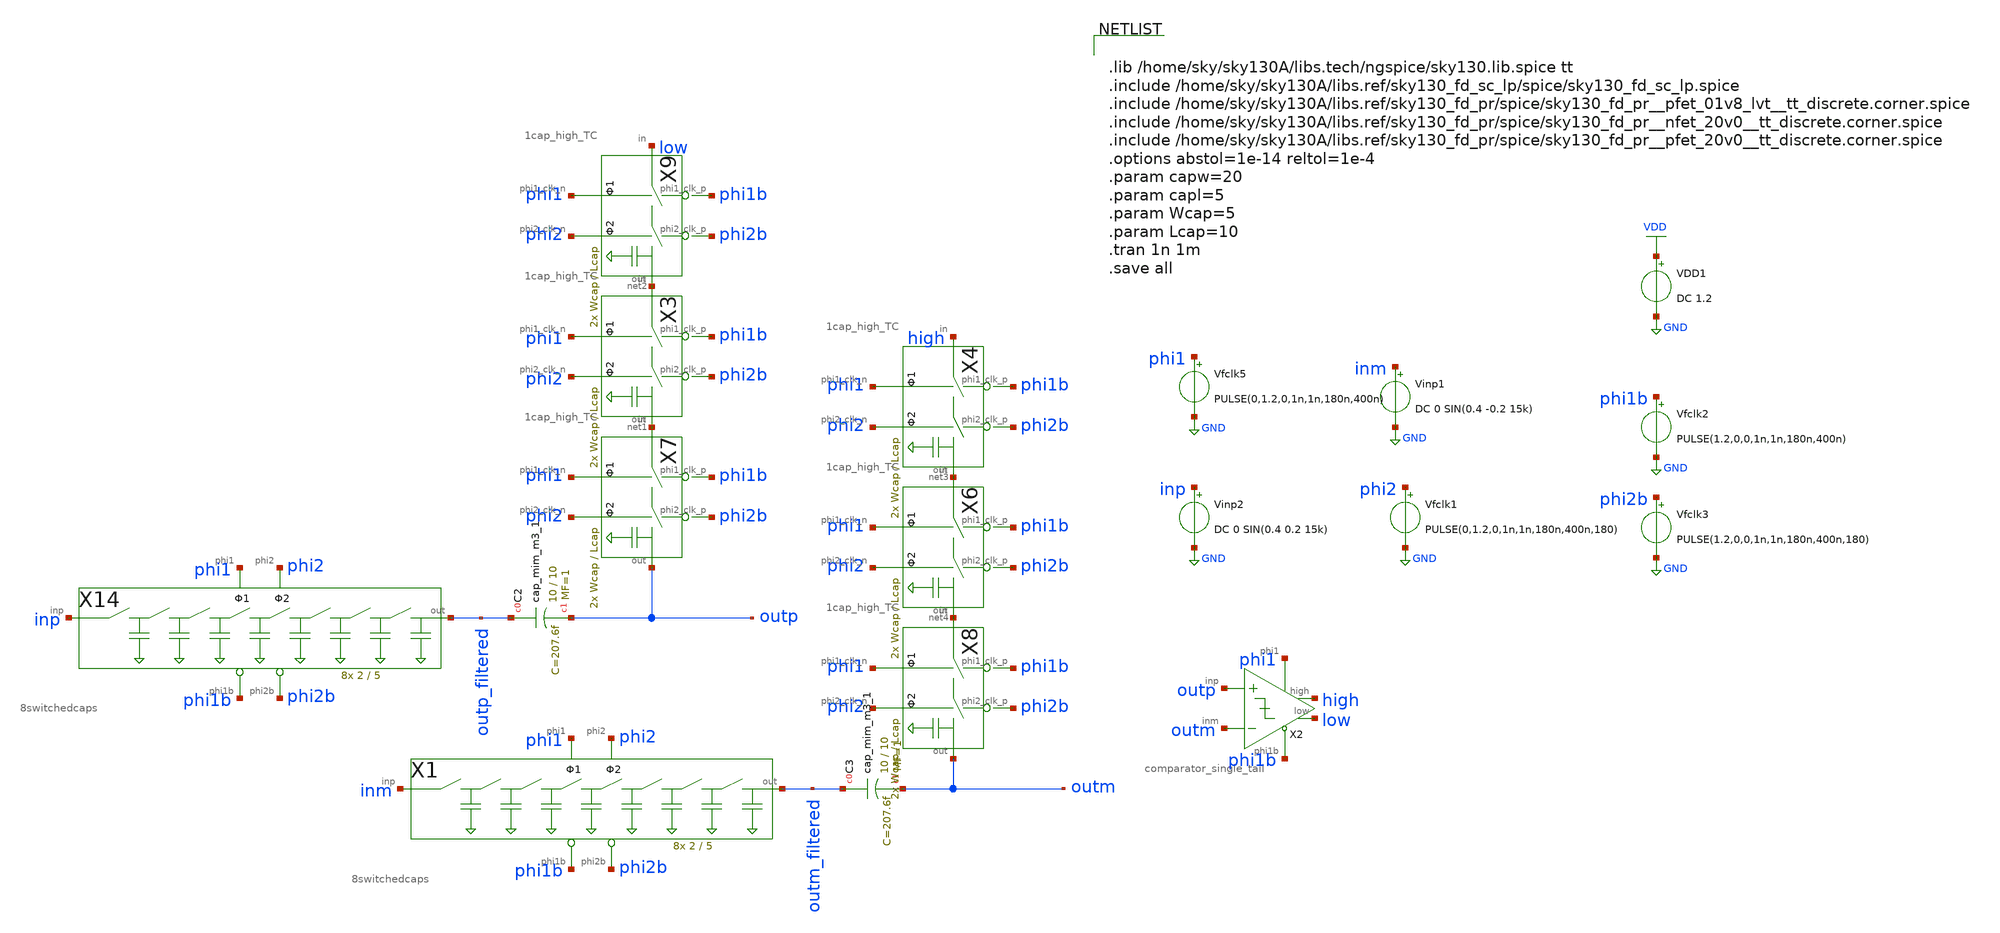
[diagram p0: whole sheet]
** sch_path: xschem/archive/comparator_latest/3cao_com_tb_az.sch
**.subckt 3cao_com_tb_az
VDD1 VDD GND DC 1.2
Vfclk5 phi1 GND PULSE(0,1.2,0,1n,1n,180n,400n)
Vfclk1 phi2 GND PULSE(0,1.2,0,1n,1n,180n,400n,180)
Vfclk2 phi1b GND PULSE(1.2,0,0,1n,1n,180n,400n)
Vfclk3 phi2b GND PULSE(1.2,0,0,1n,1n,180n,400n,180)
Vinp2 inp GND DC 0 SIN(0.4 0.2 15k)
Vinp1 inm GND DC 0 SIN(0.4 -0.2 15k)
XC2 outp_filtered outp sky130_fd_pr__cap_mim_m3_1 W=10 L=10 MF=1 m=1
XC3 outm_filtered outm sky130_fd_pr__cap_mim_m3_1 W=10 L=10 MF=1 m=1
X14 inp outp_filtered phi2 phi1 phi1b phi2b 8switchedcaps Wcap=2 Lcap=5
X1 inm outm_filtered phi2 phi1 phi1b phi2b 8switchedcaps Wcap=2 Lcap=5
X7 net1 outp phi2 phi1 phi1b phi2b 1cap_high_TC Wcap=Wcap Lcap=Lcap
X3 net2 net1 phi2 phi1 phi1b phi2b 1cap_high_TC Wcap=Wcap Lcap=Lcap
X4 high net3 phi2 phi1 phi1b phi2b 1cap_high_TC Wcap=Wcap Lcap=Lcap
X6 net3 net4 phi2 phi1 phi1b phi2b 1cap_high_TC Wcap=Wcap Lcap=Lcap
X8 net4 outm phi2 phi1 phi1b phi2b 1cap_high_TC Wcap=Wcap Lcap=Lcap
X9 low net2 phi2 phi1 phi1b phi2b 1cap_high_TC Wcap=Wcap Lcap=Lcap
X2 outp outm high phi1 phi1b low comparator_single_tail Wplus=0.42 Lplus=0.42 Wminus=0.42
+ Lminus=0.15
**** begin user architecture code


.lib /home/sky/sky130A/libs.tech/ngspice/sky130.lib.spice tt
.include /home/sky/sky130A/libs.ref/sky130_fd_sc_lp/spice/sky130_fd_sc_lp.spice
.include /home/sky/sky130A/libs.ref/sky130_fd_pr/spice/sky130_fd_pr__pfet_01v8_lvt__tt_discrete.corner.spice
.include /home/sky/sky130A/libs.ref/sky130_fd_pr/spice/sky130_fd_pr__nfet_20v0__tt_discrete.corner.spice
.include /home/sky/sky130A/libs.ref/sky130_fd_pr/spice/sky130_fd_pr__pfet_20v0__tt_discrete.corner.spice
.options abstol=1e-14 reltol=1e-4
.param capw=20
.param capl=5
.param Wcap=5
.param Lcap=10
.tran 1n 1m
.save all


**** end user architecture code
**.ends
.GLOBAL GND
.GLOBAL VDD
.end
